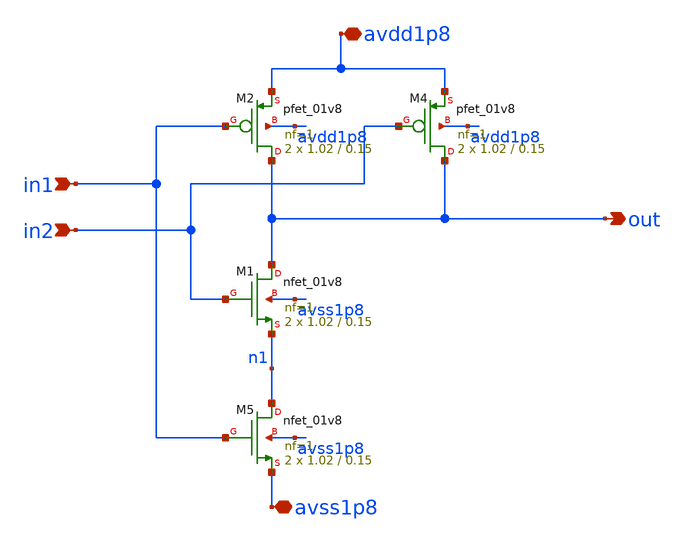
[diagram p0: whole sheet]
** sch_path: xschem/afernandez_residue_amplifier/nand_logic.sch
**.subckt nand_logic in1 in2 out avdd1p8 avss1p8
*.ipin in1
*.ipin in2
*.opin out
*.iopin avdd1p8
*.iopin avss1p8
XM4 out in2 avdd1p8 avdd1p8 sky130_fd_pr__pfet_01v8 L=0.15 W=1.02 nf=1 ad='int((nf+1)/2) * W/nf * 0.29'
+ as='int((nf+2)/2) * W/nf * 0.29' pd='2*int((nf+1)/2) * (W/nf + 0.29)' ps='2*int((nf+2)/2) * (W/nf + 0.29)'
+ nrd='0.29 / W' nrs='0.29 / W' sa=0 sb=0 sd=0 mult=2 m=2
XM5 n1 in1 avss1p8 avss1p8 sky130_fd_pr__nfet_01v8 L=0.15 W=1.02 nf=1 ad='int((nf+1)/2) * W/nf * 0.29'
+ as='int((nf+2)/2) * W/nf * 0.29' pd='2*int((nf+1)/2) * (W/nf + 0.29)' ps='2*int((nf+2)/2) * (W/nf + 0.29)'
+ nrd='0.29 / W' nrs='0.29 / W' sa=0 sb=0 sd=0 mult=2 m=2
XM1 out in2 n1 avss1p8 sky130_fd_pr__nfet_01v8 L=0.15 W=1.02 nf=1 ad='int((nf+1)/2) * W/nf * 0.29' as='int((nf+2)/2) * W/nf * 0.29'
+ pd='2*int((nf+1)/2) * (W/nf + 0.29)' ps='2*int((nf+2)/2) * (W/nf + 0.29)' nrd='0.29 / W' nrs='0.29 / W'
+ sa=0 sb=0 sd=0 mult=2 m=2
XM2 out in1 avdd1p8 avdd1p8 sky130_fd_pr__pfet_01v8 L=0.15 W=1.02 nf=1 ad='int((nf+1)/2) * W/nf * 0.29'
+ as='int((nf+2)/2) * W/nf * 0.29' pd='2*int((nf+1)/2) * (W/nf + 0.29)' ps='2*int((nf+2)/2) * (W/nf + 0.29)'
+ nrd='0.29 / W' nrs='0.29 / W' sa=0 sb=0 sd=0 mult=2 m=2
**.ends
.end
